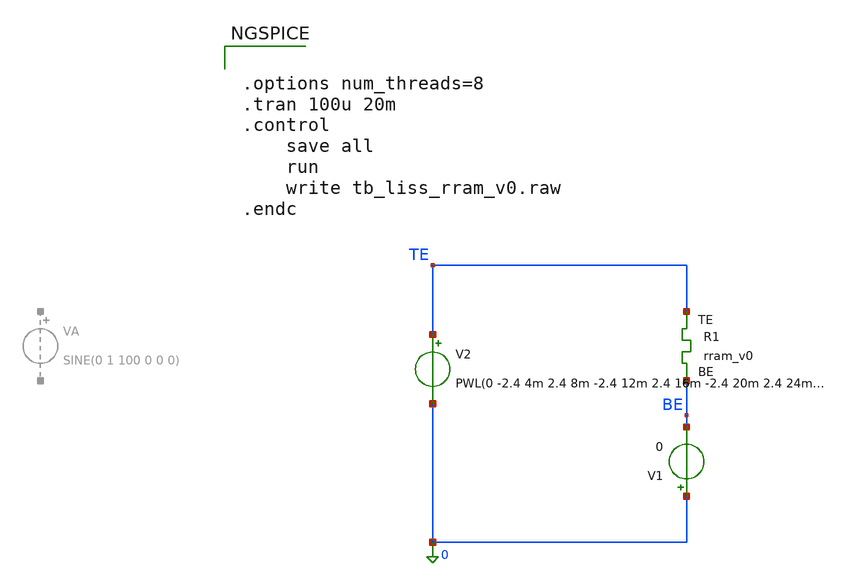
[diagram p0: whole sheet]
** sch_path: memristor_models/wellposed/tb_liss_rram_v0.sch
**.subckt tb_liss_rram_v0
XR1 TE BE rram_v0
V1 0 BE 0
V2 TE 0 PWL(0 -2.4 4m 2.4 8m -2.4 12m 2.4 16m -2.4 20m 2.4 24m -2.4)
**** begin user architecture code


.options num_threads=8
.tran 100u 20m
.control
	save all
	run
	write tb_liss_rram_v0.raw
.endc




** opencircuitdesign pdks install
.inc $::SKYWATER_MODELS/rram_v0.spice

**** end user architecture code
**.ends
.end
